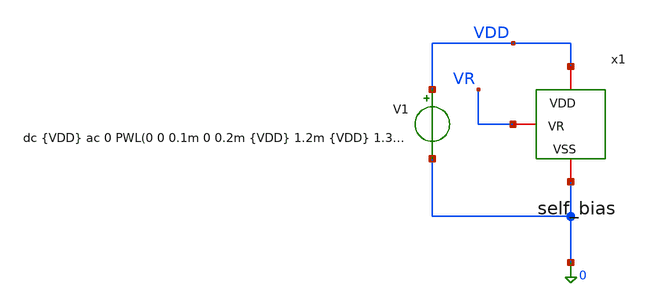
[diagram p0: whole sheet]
** sch_path: xschem/Self_Bias/self_bias_tb_mc.sch
**.subckt self_bias_tb_mc
V1 VDD 0 dc {VDD} ac 0 PWL(0 0 0.1m 0 0.2m {VDD} 1.2m {VDD} 1.3m 0 2m 0 3m {VDD} 4m {VDD} 4.1m 0 5m 0
+ 105m {VDD} 110m {VDD} 110.1m 0)
x1 VDD VR 0 self_bias
**** begin user architecture code


* ==============================================================================
* ENCABEZADO DEL ARCHIVO:
* Script de simulación Monte Carlo (Mismatch) para el circuito Self-Bias.
* Evalúa las 3 rampas de arranque (Trise = 100us, 1ms y 100ms) con tiempos de
* espera recortados (110.1ms totales en lugar de 410ms).
* ==============================================================================

* 1. Librería de modelos Sky130 con Mismatch (Monte Carlo)
.lib /foss/pdks/sky130A/libs.tech/ngspice/sky130.lib.spice tt_mm

.option temp=27
.option num_threads=8

* 2. Parámetros globales
.param VDD = 1.8
.param rsh_var = agauss(0, 0.005, 1)

.control
let mc_runs = 100
let run = 1

set appendwrite
set filetype=ascii

echo === INICIO MONTE CARLO SELF BIAS === > self_bias_mc.txt

while run <= mc_runs

    echo ======================================
    echo CORRIENDO MONTE CARLO ITERACION: $&run
    echo ======================================
    echo --- ITERACION: $&run --- >> self_bias_mc.txt

    * 1. Resetear variables aleatorias y guardar solo las señales necesarias
    reset
    save v(VDD) v(vr) @m.x1.xMp4.msky130_fd_pr__pfet_01v8_lvt[id]

    * 2. Análisis Transitorio corto (110.1ms totales para las 3 rampas)
    tran 1m 110.1m

    write self_bias_mc_tran.raw v(VDD) v(vr) @m.x1.xMp4.msky130_fd_pr__pfet_01v8_lvt[id]

    * 3. Mediciones en las 3 rampas
    * --- PULSO 1 (Trise = 100us: sube de 0.1m a 0.2m, medimos en 1ms) ---
    meas tran vr_100us FIND v(vr) AT=1m
    meas tran id_100us FIND @m.x1.xMp4.msky130_fd_pr__pfet_01v8_lvt[id] AT=1m

    * --- PULSO 2 (Trise = 1ms: sube de 2m a 3m, medimos en 3.8ms) ---
    meas tran vr_1ms FIND v(vr) AT=3.8m
    meas tran id_1ms FIND @m.x1.xMp4.msky130_fd_pr__pfet_01v8_lvt[id] AT=3.8m

    * --- PULSO 3 (Trise = 100ms: sube de 5m a 105m, medimos en 108ms) ---
    meas tran vr_100ms FIND v(vr) AT=108m
    meas tran id_100ms FIND @m.x1.xMp4.msky130_fd_pr__pfet_01v8_lvt[id] AT=108m

    * Convertir corrientes a microamperios (uA)
    let id_uA_100us = id_100us * 1000000
    let id_uA_1ms   = id_1ms * 1000000
    let id_uA_100ms = id_100ms * 1000000

    * 4. Guardar resultados en el archivo de texto
    echo 'Resultados Iteración $&run:' >> self_bias_mc.txt
    echo '  [100us] VR = $&vr_100us V   | IBIAS = $&id_uA_100us uA' >> self_bias_mc.txt
    echo '  [1ms]   VR = $&vr_1ms V     | IBIAS = $&id_uA_1ms uA' >> self_bias_mc.txt
    echo '  [100ms] VR = $&vr_100ms V   | IBIAS = $&id_uA_100ms uA' >> self_bias_mc.txt
    echo '--------------------------------------' >> self_bias_mc.txt

    let run = run + 1

end

echo === FIN MONTE CARLO SELF BIAS === >> self_bias_mc.txt

.endc


**** end user architecture code
**.ends

* expanding   symbol:  /foss/designs/LDO-sky130/xschem/Self_Bias/self_bias.sym # of pins=3
** sym_path: xschem/Iref/self_bias.sym
** sch_path: xschem/Iref/self_bias.sch
.subckt self_bias VDD VR VSS
*.iopin VR
*.iopin VDD
*.iopin VSS
XMp4 vgp_self vgp_self VDD VDD sky130_fd_pr__pfet_01v8_lvt L=1 W=30 nf=6 ad='int((6 + 1)/2) * 30 / 6 * 0.29'
+ as='int((6 + 2)/2) * 30 / 6 * 0.29' pd='2*int((6 + 1)/2) * (30 / 6 + 0.29)' ps='2*int((6 + 2)/2) * (30 / 6 + 0.29)'
+ nrd='0.29 / 30 ' nrs='0.29 / 30 ' sa=0 sb=0 sd=0 mult=1 m=1
XMp3 VDI vgp_self VDD VDD sky130_fd_pr__pfet_01v8_lvt L=1 W=30 nf=6 ad='int((6 + 1)/2) * 30 / 6 * 0.29'
+ as='int((6 + 2)/2) * 30 / 6 * 0.29' pd='2*int((6 + 1)/2) * (30 / 6 + 0.29)' ps='2*int((6 + 2)/2) * (30 / 6 + 0.29)'
+ nrd='0.29 / 30 ' nrs='0.29 / 30 ' sa=0 sb=0 sd=0 mult=1 m=1
XMs2 VDinv VR vp1 VDD sky130_fd_pr__pfet_01v8_lvt L=5 W=0.5 nf=1 ad='int((1 + 1)/2) * 0.5 / 1 * 0.29'
+ as='int((1 + 2)/2) * 0.5 / 1 * 0.29' pd='2*int((1 + 1)/2) * (0.5 / 1 + 0.29)' ps='2*int((1 + 2)/2) * (0.5 / 1 + 0.29)'
+ nrd='0.29 / 0.5 ' nrs='0.29 / 0.5 ' sa=0 sb=0 sd=0 mult=1 m=1
XMn2 vgp_self VDI VR VSS sky130_fd_pr__nfet_01v8 L=1 W=24 nf=6 ad='int((6 + 1)/2) * 24 / 6 * 0.29' as='int((6 + 2)/2) * 24 / 6 * 0.29'
+ pd='2*int((6 + 1)/2) * (24 / 6 + 0.29)' ps='2*int((6 + 2)/2) * (24 / 6 + 0.29)' nrd='0.29 / 24 ' nrs='0.29 / 24 '
+ sa=0 sb=0 sd=0 mult=1 m=1
XMn1 VDI VR VSS VSS sky130_fd_pr__nfet_01v8 L=1 W=5 nf=5 ad='int((5 + 1)/2) * 5 / 5 * 0.29' as='int((5 + 2)/2) * 5 / 5 * 0.29'
+ pd='2*int((5 + 1)/2) * (5 / 5 + 0.29)' ps='2*int((5 + 2)/2) * (5 / 5 + 0.29)' nrd='0.29 / 5 ' nrs='0.29 / 5 '
+ sa=0 sb=0 sd=0 mult=1 m=1
XMs3 VDinv VR VSS VSS sky130_fd_pr__nfet_01v8 L=1 W=20 nf=5 ad='int((5 + 1)/2) * 20 / 5 * 0.29' as='int((5 + 2)/2) * 20 / 5 * 0.29'
+ pd='2*int((5 + 1)/2) * (20 / 5 + 0.29)' ps='2*int((5 + 2)/2) * (20 / 5 + 0.29)' nrd='0.29 / 20 ' nrs='0.29 / 20 '
+ sa=0 sb=0 sd=0 mult=1 m=1
XMs1 vgp_self VDinv VSS VSS sky130_fd_pr__nfet_01v8 L=1 W=2 nf=2 ad='int((2 + 1)/2) * 2 / 2 * 0.29' as='int((2 + 2)/2) * 2 / 2 * 0.29'
+ pd='2*int((2 + 1)/2) * (2 / 2 + 0.29)' ps='2*int((2 + 2)/2) * (2 / 2 + 0.29)' nrd='0.29 / 2 ' nrs='0.29 / 2 '
+ sa=0 sb=0 sd=0 mult=1 m=1
XR11 VSS VR VSS sky130_fd_pr__res_xhigh_po_0p69 L=20.7 mult=1 m=1
XMs4 vp1 VR vp2 VDD sky130_fd_pr__pfet_01v8_lvt L=5 W=0.5 nf=1 ad='int((1 + 1)/2) * 0.5 / 1 * 0.29' as='int((1 + 2)/2) * 0.5 / 1 * 0.29'
+ pd='2*int((1 + 1)/2) * (0.5 / 1 + 0.29)' ps='2*int((1 + 2)/2) * (0.5 / 1 + 0.29)' nrd='0.29 / 0.5 ' nrs='0.29 / 0.5 '
+ sa=0 sb=0 sd=0 mult=1 m=1
XMs5 vp2 VR vp3 VDD sky130_fd_pr__pfet_01v8_lvt L=5 W=0.5 nf=1 ad='int((1 + 1)/2) * 0.5 / 1 * 0.29' as='int((1 + 2)/2) * 0.5 / 1 * 0.29'
+ pd='2*int((1 + 1)/2) * (0.5 / 1 + 0.29)' ps='2*int((1 + 2)/2) * (0.5 / 1 + 0.29)' nrd='0.29 / 0.5 ' nrs='0.29 / 0.5 '
+ sa=0 sb=0 sd=0 mult=1 m=1
XMs6 vp3 VR vp4 VDD sky130_fd_pr__pfet_01v8_lvt L=5 W=0.5 nf=1 ad='int((1 + 1)/2) * 0.5 / 1 * 0.29' as='int((1 + 2)/2) * 0.5 / 1 * 0.29'
+ pd='2*int((1 + 1)/2) * (0.5 / 1 + 0.29)' ps='2*int((1 + 2)/2) * (0.5 / 1 + 0.29)' nrd='0.29 / 0.5 ' nrs='0.29 / 0.5 '
+ sa=0 sb=0 sd=0 mult=1 m=1
XMs7 vp4 VR VDD VDD sky130_fd_pr__pfet_01v8_lvt L=5 W=0.5 nf=1 ad='int((1 + 1)/2) * 0.5 / 1 * 0.29' as='int((1 + 2)/2) * 0.5 / 1 * 0.29'
+ pd='2*int((1 + 1)/2) * (0.5 / 1 + 0.29)' ps='2*int((1 + 2)/2) * (0.5 / 1 + 0.29)' nrd='0.29 / 0.5 ' nrs='0.29 / 0.5 '
+ sa=0 sb=0 sd=0 mult=1 m=1
.ends

.end
